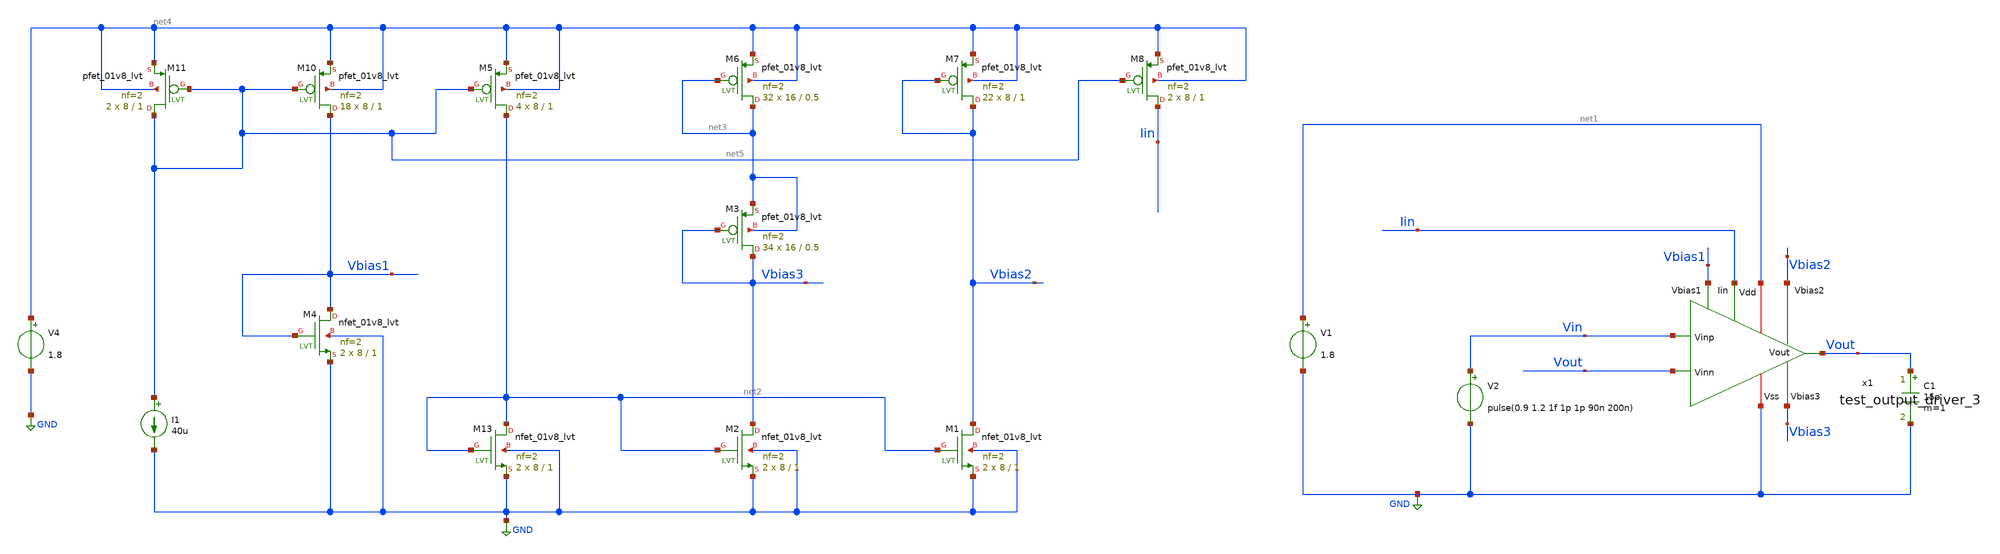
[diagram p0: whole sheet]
** sch_path: xschem/ip_block/opamp/folded_cas_xiaoyi/tb_output_swing_output_driver_3.sch
**.subckt tb_output_swing_output_driver_3
V1 net1 GND 1.8
C1 Vout GND 15p m=1
XM2 Vbias3 net2 GND GND sky130_fd_pr__nfet_01v8_lvt L=1 W=8 nf=2 ad='int((nf+1)/2) * W/nf * 0.29' as='int((nf+2)/2) * W/nf * 0.29'
+ pd='2*int((nf+1)/2) * (W/nf + 0.29)' ps='2*int((nf+2)/2) * (W/nf + 0.29)' nrd='0.29 / W' nrs='0.29 / W'
+ sa=0 sb=0 sd=0 mult=2 m=2
XM3 Vbias3 Vbias3 net3 net3 sky130_fd_pr__pfet_01v8_lvt L=0.5 W=16 nf=2 ad='int((nf+1)/2) * W/nf * 0.29'
+ as='int((nf+2)/2) * W/nf * 0.29' pd='2*int((nf+1)/2) * (W/nf + 0.29)' ps='2*int((nf+2)/2) * (W/nf + 0.29)'
+ nrd='0.29 / W' nrs='0.29 / W' sa=0 sb=0 sd=0 mult=34 m=34
I1 net5 GND 40u
XM4 Vbias1 Vbias1 GND GND sky130_fd_pr__nfet_01v8_lvt L=1 W=8 nf=2 ad='int((nf+1)/2) * W/nf * 0.29' as='int((nf+2)/2) * W/nf * 0.29'
+ pd='2*int((nf+1)/2) * (W/nf + 0.29)' ps='2*int((nf+2)/2) * (W/nf + 0.29)' nrd='0.29 / W' nrs='0.29 / W'
+ sa=0 sb=0 sd=0 mult=2 m=2
V4 net4 GND 1.8
XM1 Vbias2 net2 GND GND sky130_fd_pr__nfet_01v8_lvt L=1 W=8 nf=2 ad='int((nf+1)/2) * W/nf * 0.29' as='int((nf+2)/2) * W/nf * 0.29'
+ pd='2*int((nf+1)/2) * (W/nf + 0.29)' ps='2*int((nf+2)/2) * (W/nf + 0.29)' nrd='0.29 / W' nrs='0.29 / W'
+ sa=0 sb=0 sd=0 mult=2 m=2
XM6 net3 net3 net4 net4 sky130_fd_pr__pfet_01v8_lvt L=0.5 W=16 nf=2 ad='int((nf+1)/2) * W/nf * 0.29'
+ as='int((nf+2)/2) * W/nf * 0.29' pd='2*int((nf+1)/2) * (W/nf + 0.29)' ps='2*int((nf+2)/2) * (W/nf + 0.29)'
+ nrd='0.29 / W' nrs='0.29 / W' sa=0 sb=0 sd=0 mult=32 m=32
XM7 Vbias2 Vbias2 net4 net4 sky130_fd_pr__pfet_01v8_lvt L=1 W=8 nf=2 ad='int((nf+1)/2) * W/nf * 0.29'
+ as='int((nf+2)/2) * W/nf * 0.29' pd='2*int((nf+1)/2) * (W/nf + 0.29)' ps='2*int((nf+2)/2) * (W/nf + 0.29)'
+ nrd='0.29 / W' nrs='0.29 / W' sa=0 sb=0 sd=0 mult=22 m=22
XM5 net2 net5 net4 net4 sky130_fd_pr__pfet_01v8_lvt L=1 W=8 nf=2 ad='int((nf+1)/2) * W/nf * 0.29' as='int((nf+2)/2) * W/nf * 0.29'
+ pd='2*int((nf+1)/2) * (W/nf + 0.29)' ps='2*int((nf+2)/2) * (W/nf + 0.29)' nrd='0.29 / W' nrs='0.29 / W'
+ sa=0 sb=0 sd=0 mult=4 m=4
XM10 Vbias1 net5 net4 net4 sky130_fd_pr__pfet_01v8_lvt L=1 W=8 nf=2 ad='int((nf+1)/2) * W/nf * 0.29'
+ as='int((nf+2)/2) * W/nf * 0.29' pd='2*int((nf+1)/2) * (W/nf + 0.29)' ps='2*int((nf+2)/2) * (W/nf + 0.29)'
+ nrd='0.29 / W' nrs='0.29 / W' sa=0 sb=0 sd=0 mult=18 m=18
XM11 net5 net5 net4 net4 sky130_fd_pr__pfet_01v8_lvt L=1 W=8 nf=2 ad='int((nf+1)/2) * W/nf * 0.29' as='int((nf+2)/2) * W/nf * 0.29'
+ pd='2*int((nf+1)/2) * (W/nf + 0.29)' ps='2*int((nf+2)/2) * (W/nf + 0.29)' nrd='0.29 / W' nrs='0.29 / W'
+ sa=0 sb=0 sd=0 mult=2 m=2
XM13 net2 net2 GND GND sky130_fd_pr__nfet_01v8_lvt L=1 W=8 nf=2 ad='int((nf+1)/2) * W/nf * 0.29' as='int((nf+2)/2) * W/nf * 0.29'
+ pd='2*int((nf+1)/2) * (W/nf + 0.29)' ps='2*int((nf+2)/2) * (W/nf + 0.29)' nrd='0.29 / W' nrs='0.29 / W'
+ sa=0 sb=0 sd=0 mult=2 m=2
x1 net1 Vout Vin Vout Iin GND Vbias1 Vbias2 Vbias3 test_output_driver_3
V2 Vin GND pulse(0.9 1.2 1f 1p 1p 90n 200n)
XM8 Iin net5 net4 net4 sky130_fd_pr__pfet_01v8_lvt L=1 W=8 nf=2 ad='int((nf+1)/2) * W/nf * 0.29' as='int((nf+2)/2) * W/nf * 0.29'
+ pd='2*int((nf+1)/2) * (W/nf + 0.29)' ps='2*int((nf+2)/2) * (W/nf + 0.29)' nrd='0.29 / W' nrs='0.29 / W'
+ sa=0 sb=0 sd=0 mult=2 m=2
**** begin user architecture code
.lib $::SKYWATER_MODELS/sky130.lib.spice tt


.option temp=70
.op
*.ac dec 10 1 1G
.tran 0.1n 1u

.control
*ac dec 10 1 1G
tran 0.1n 1u
*ac dec 10 1 1G
*let phase = 180/PI*vp(Vout)

*plot vdb(Vout) phase
plot Vin Vout
.endc

.save all



**** end user architecture code
**.ends
.GLOBAL GND
.end
